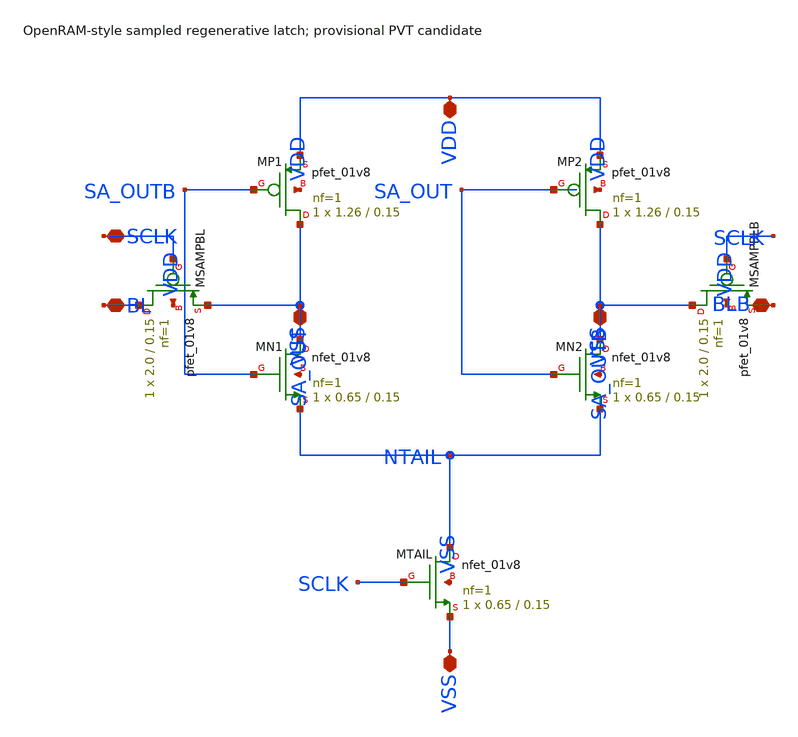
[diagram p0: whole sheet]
** sch_path: cells/sense_amp.sch
**.subckt sense_amp VDD VSS BL BLB SCLK SA_OUT SA_OUTB
*.iopin VDD
*.iopin VSS
*.iopin BL
*.iopin BLB
*.iopin SCLK
*.iopin SA_OUT
*.iopin SA_OUTB
XMP1 SA_OUT SA_OUTB VDD VDD sky130_fd_pr__pfet_01v8 L=0.15 W=1.26 nf=1 ad='int((nf+1)/2) * W/nf * 0.29'
+ as='int((nf+2)/2) * W/nf * 0.29' pd='2*int((nf+1)/2) * (W/nf + 0.29)' ps='2*int((nf+2)/2) * (W/nf + 0.29)'
+ nrd='0.29 / W' nrs='0.29 / W' sa=0 sb=0 sd=0 mult=1 m=1
XMN1 SA_OUT SA_OUTB NTAIL VSS sky130_fd_pr__nfet_01v8 L=0.15 W=0.65 nf=1 ad='int((1 + 1)/2) * 0.65 / 1 * 0.29'
+ as='int((1 + 2)/2) * 0.65 / 1 * 0.29' pd='2*int((1 + 1)/2) * (0.65 / 1 + 0.29)' ps='2*int((1 + 2)/2) * (0.65 / 1 + 0.29)'
+ nrd='0.29 / 0.65 ' nrs='0.29 / 0.65 ' sa=0 sb=0 sd=0 mult=1 m=1
XMP2 SA_OUTB SA_OUT VDD VDD sky130_fd_pr__pfet_01v8 L=0.15 W=1.26 nf=1 ad='int((nf+1)/2) * W/nf * 0.29'
+ as='int((nf+2)/2) * W/nf * 0.29' pd='2*int((nf+1)/2) * (W/nf + 0.29)' ps='2*int((nf+2)/2) * (W/nf + 0.29)'
+ nrd='0.29 / W' nrs='0.29 / W' sa=0 sb=0 sd=0 mult=1 m=1
XMN2 SA_OUTB SA_OUT NTAIL VSS sky130_fd_pr__nfet_01v8 L=0.15 W=0.65 nf=1 ad='int((1 + 1)/2) * 0.65 / 1 * 0.29'
+ as='int((1 + 2)/2) * 0.65 / 1 * 0.29' pd='2*int((1 + 1)/2) * (0.65 / 1 + 0.29)' ps='2*int((1 + 2)/2) * (0.65 / 1 + 0.29)'
+ nrd='0.29 / 0.65 ' nrs='0.29 / 0.65 ' sa=0 sb=0 sd=0 mult=1 m=1
XMSAMPBL BL SCLK SA_OUT VDD sky130_fd_pr__pfet_01v8 L=0.15 W=2.0 nf=1 ad='int((nf+1)/2) * W/nf * 0.29'
+ as='int((nf+2)/2) * W/nf * 0.29' pd='2*int((nf+1)/2) * (W/nf + 0.29)' ps='2*int((nf+2)/2) * (W/nf + 0.29)'
+ nrd='0.29 / W' nrs='0.29 / W' sa=0 sb=0 sd=0 mult=1 m=1
XMSAMPBLB SA_OUTB SCLK BLB VDD sky130_fd_pr__pfet_01v8 L=0.15 W=2.0 nf=1 ad='int((nf+1)/2) * W/nf * 0.29'
+ as='int((nf+2)/2) * W/nf * 0.29' pd='2*int((nf+1)/2) * (W/nf + 0.29)' ps='2*int((nf+2)/2) * (W/nf + 0.29)'
+ nrd='0.29 / W' nrs='0.29 / W' sa=0 sb=0 sd=0 mult=1 m=1
XMTAIL NTAIL SCLK VSS VSS sky130_fd_pr__nfet_01v8 L=0.15 W=0.65 nf=1 ad='int((1 + 1)/2) * 0.65 / 1 * 0.29'
+ as='int((1 + 2)/2) * 0.65 / 1 * 0.29' pd='2*int((1 + 1)/2) * (0.65 / 1 + 0.29)' ps='2*int((1 + 2)/2) * (0.65 / 1 + 0.29)'
+ nrd='0.29 / 0.65 ' nrs='0.29 / 0.65 ' sa=0 sb=0 sd=0 mult=1 m=1
**.ends
.end
